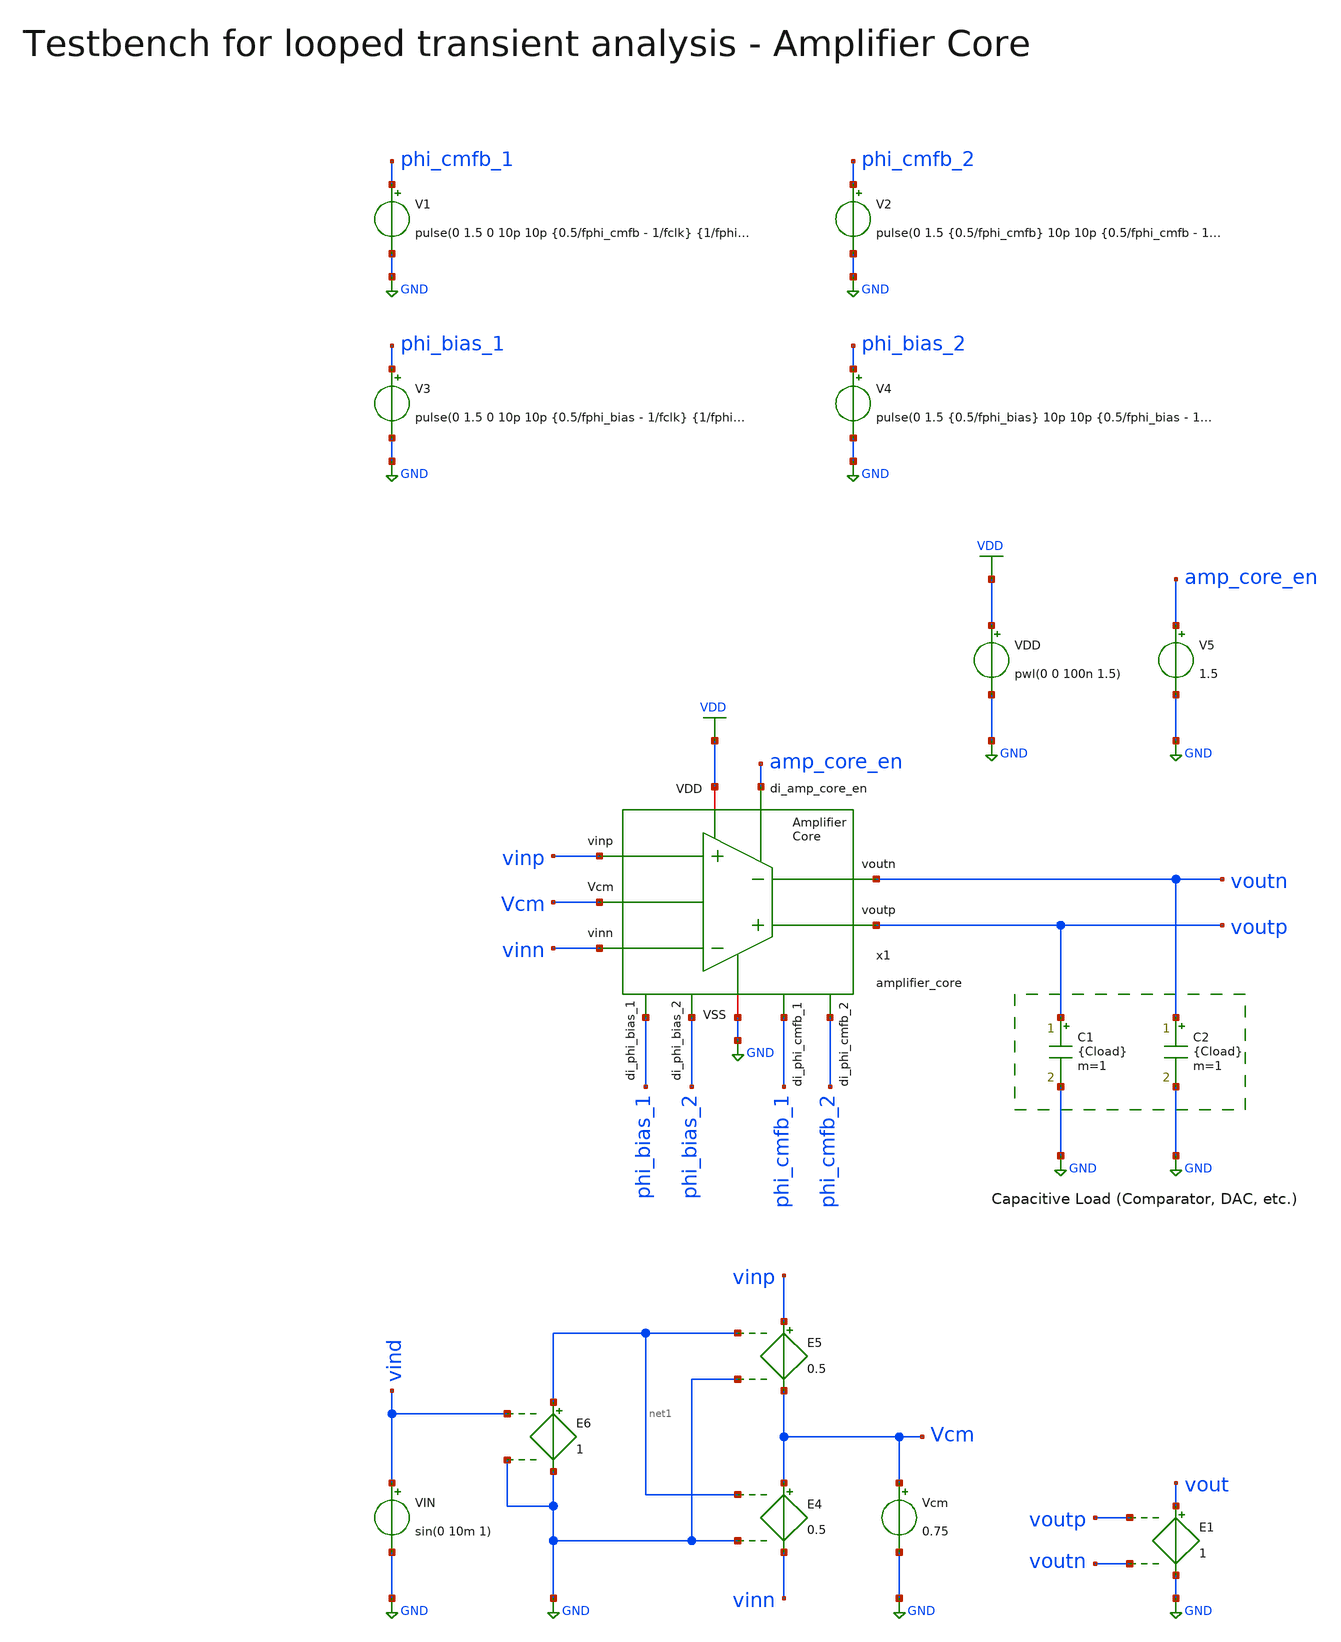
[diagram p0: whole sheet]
** sch_path: SG13G2_ATBS-ADC-main/xschem/bio_amplifier/amplifier_core/testbenches/amplifier_core_tb_looped_tran_ol.sch
**.subckt amplifier_core_tb_looped_tran_ol
C1 voutp GND {Cload} m=1
C2 voutn GND {Cload} m=1
V1 phi_cmfb_1 GND pulse(0 1.5 0 10p 10p {0.5/fphi_cmfb - 1/fclk} {1/fphi_cmfb})
Vcm Vcm GND 0.75
E4 Vcm vinn net1 GND 0.5
E5 vinp Vcm net1 GND 0.5
E6 net1 GND vind GND 1
V2 phi_cmfb_2 GND pulse(0 1.5 {0.5/fphi_cmfb} 10p 10p {0.5/fphi_cmfb - 1/fclk} {1/fphi_cmfb})
V3 phi_bias_1 GND pulse(0 1.5 0 10p 10p {0.5/fphi_bias - 1/fclk} {1/fphi_bias})
V4 phi_bias_2 GND pulse(0 1.5 {0.5/fphi_bias} 10p 10p {0.5/fphi_bias - 1/fclk} {1/fphi_bias})
V5 amp_core_en GND 1.5
VIN vind GND sin(0 10m 1)
E1 vout GND voutp voutn 1
x1 phi_cmfb_1 phi_bias_2 phi_bias_1 phi_cmfb_2 voutp voutn amp_core_en vinn vinp VDD GND Vcm
+ amplifier_core
VDD VDD GND pwl(0 0 100n 1.5)
**** begin user architecture code

.lib cornerMOSlv.lib mos_tt
.lib cornerMOShv.lib mos_tt
.lib cornerRES.lib res_typ



.param temp=27
* 228fF DAC + (1 - beta) * 3.3pF
.param Cload=3.49p
.param fclk=8000000
.csparam fclk=fclk
.param fphi_cmfb=62500
.param fphi_bias=62500
.options klu method=gear reltol=1e-2 abstol=1e-15 gmin=1e-15
.control

save vind vinp vinn voutp voutn vout
setplot const
set wr_vecnames
set wr_singlescale

* User constants
let tstart = 500u
let fstart = 10k
let fstop = 10k
let amount_of_periods = 2
let points_per_period = 10
let points_per_dec = 1
let vamp = 1m

* Generate a logarithmic frequency vector
compose freq_vec dec=$&const.points_per_dec start=$&const.fstart stop=$&const.fstop

* Generate gain and phase vectors
let Aol_dB_vec = freq_vec
let phase_vec = freq_vec

* Loop index
let idx = 0

* For-Loop
foreach freq_val $&freq_vec
  * 10 data points per period
  * let tstep = 1/($&const.points_per_period*$freq_val)
  let tstep = 1/fclk

  * 2 periods long
  let tstop = ($&const.amount_of_periods * 1/$freq_val) + $&const.tstart

  * Alter input sine frequency
  alter @VIN[SIN] = [ 0 $&const.vamp $freq_val 0 0 0 ]

  * Transient Analysis
  tran $&tstep $&tstop $&tstart
  write amplifier_core_tb_looped_tran_ol.raw
  set appendwrite

  * Measure maximum voltage of input
  meas tran vind_peak_peak PP v(vind) from=$&tstart to=$&tstop
  let vind_peak = vind_peak_peak / 2

  * Measure time at maximum voltage of input
  meas tran t_vind_peak MAX_AT v(vind) from=$&tstart to=$&tstop

  * Measure maximum voltage of output
  meas tran vout_peak_peak PP v(vout) from=$&tstart to=$&tstop
  let vout_peak = vout_peak_peak / 2

  * Measure time at maximum voltage of output
  meas tran t_vout_peak MAX_AT v(vout) from=$&tstart to=$&tstop

  * Calculate gain
  let Aol = vout_peak / vind_peak
  let Aol_dB = vdb(Aol)

  * Calculate phase
  let phase = (t_vout_peak - t_vind_peak) * $freq_val * 360

  * Append to vector
  let const.Aol_dB_vec[const.idx] = Aol_dB
  let const.phase_vec[const.idx] = phase

  * Update index
  let const.idx = const.idx + 1
  echo ======================================================
end

print const.Aol_dB_vec
print const.phase_vec

* Setscale for plot against frequency
setscale const.Aol_dB_vec const.freq_vec
setscale const.phase_vec const.freq_vec

* Plot open-loop gain and phase vs. frequency
plot xlog const.Aol_dB_vec title 'Open-loop gain' ylabel 'dB'
plot xlog const.phase_vec title 'Phase' ylabel 'deg'

* Write Data
wrdata
+ /foss/designs/SG13G2_ATBS-ADC-main/python/plot_simulations/data/bio_amplifier_tb_looped_tran_cl.txt const.freq_vec const.Aol_dB_vec const.phase_vec

*quit
.endc


**** end user architecture code
**.ends
.GLOBAL GND
.GLOBAL VDD
.end
